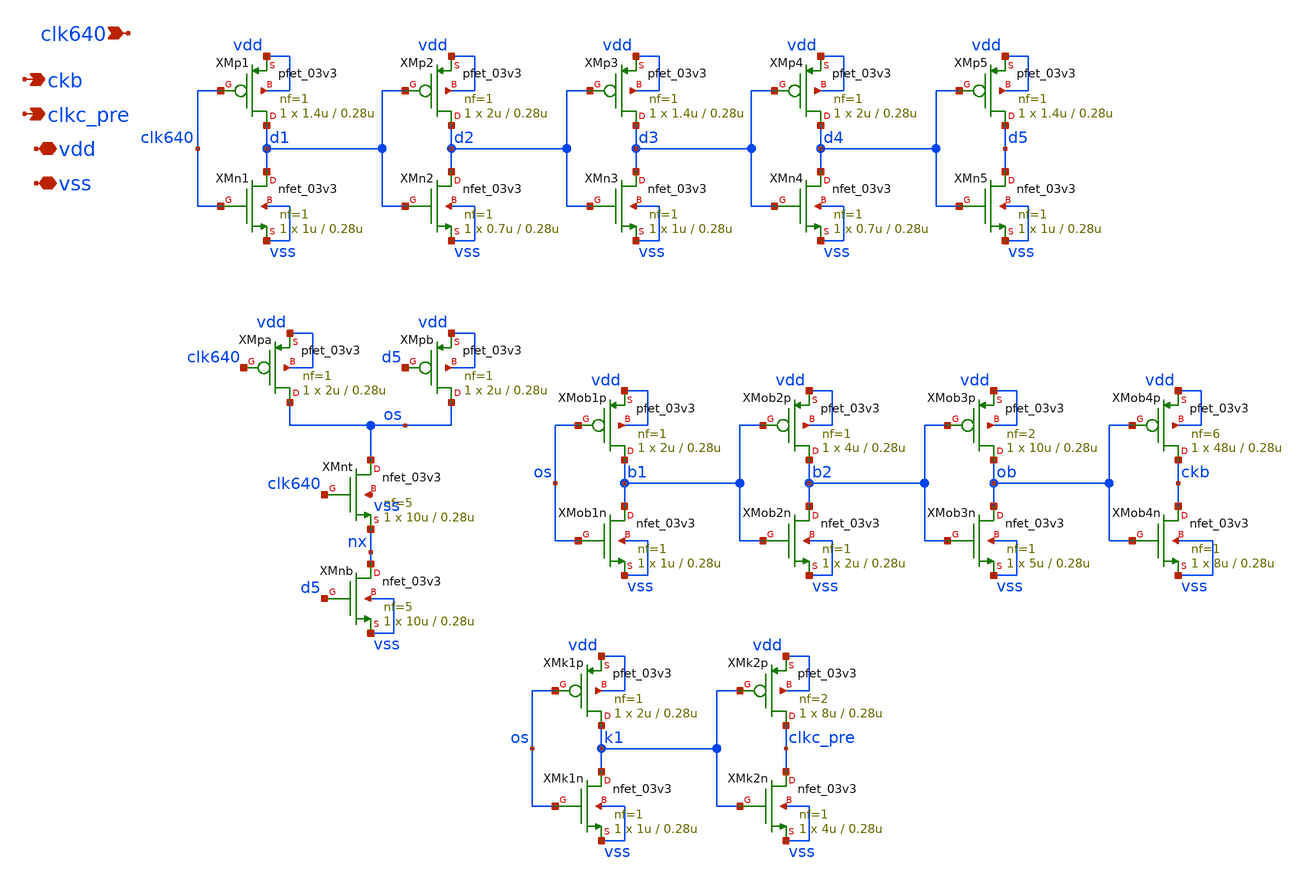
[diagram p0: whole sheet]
** sch_path: blocks/adc/comp-array/compact/clkshaper.sch
**.subckt clkshaper ckb vdd vss clkc_pre clk640
*.opin ckb
*.iopin vdd
*.iopin vss
*.opin clkc_pre
*.ipin clk640
XMn1 d1 clk640 vss vss nfet_03v3 L=0.28u W=1u nf=1 ad='int((nf+1)/2) * W/nf * 0.18u' as='int((nf+2)/2) * W/nf * 0.18u'
+ pd='2*int((nf+1)/2) * (W/nf + 0.18u)' ps='2*int((nf+2)/2) * (W/nf + 0.18u)' nrd='0.18u / W' nrs='0.18u / W'
+ sa=0 sb=0 sd=0 m=1
XMp1 d1 clk640 vdd vdd pfet_03v3 L=0.28u W=1.4u nf=1 ad='int((nf+1)/2) * W/nf * 0.18u' as='int((nf+2)/2) * W/nf * 0.18u'
+ pd='2*int((nf+1)/2) * (W/nf + 0.18u)' ps='2*int((nf+2)/2) * (W/nf + 0.18u)' nrd='0.18u / W' nrs='0.18u / W'
+ sa=0 sb=0 sd=0 m=1
XMn2 d2 d1 vss vss nfet_03v3 L=0.28u W=0.7u nf=1 ad='int((nf+1)/2) * W/nf * 0.18u' as='int((nf+2)/2) * W/nf * 0.18u'
+ pd='2*int((nf+1)/2) * (W/nf + 0.18u)' ps='2*int((nf+2)/2) * (W/nf + 0.18u)' nrd='0.18u / W' nrs='0.18u / W'
+ sa=0 sb=0 sd=0 m=1
XMp2 d2 d1 vdd vdd pfet_03v3 L=0.28u W=2u nf=1 ad='int((nf+1)/2) * W/nf * 0.18u' as='int((nf+2)/2) * W/nf * 0.18u'
+ pd='2*int((nf+1)/2) * (W/nf + 0.18u)' ps='2*int((nf+2)/2) * (W/nf + 0.18u)' nrd='0.18u / W' nrs='0.18u / W'
+ sa=0 sb=0 sd=0 m=1
XMn3 d3 d2 vss vss nfet_03v3 L=0.28u W=1u nf=1 ad='int((nf+1)/2) * W/nf * 0.18u' as='int((nf+2)/2) * W/nf * 0.18u'
+ pd='2*int((nf+1)/2) * (W/nf + 0.18u)' ps='2*int((nf+2)/2) * (W/nf + 0.18u)' nrd='0.18u / W' nrs='0.18u / W'
+ sa=0 sb=0 sd=0 m=1
XMp3 d3 d2 vdd vdd pfet_03v3 L=0.28u W=1.4u nf=1 ad='int((nf+1)/2) * W/nf * 0.18u' as='int((nf+2)/2) * W/nf * 0.18u'
+ pd='2*int((nf+1)/2) * (W/nf + 0.18u)' ps='2*int((nf+2)/2) * (W/nf + 0.18u)' nrd='0.18u / W' nrs='0.18u / W'
+ sa=0 sb=0 sd=0 m=1
XMn4 d4 d3 vss vss nfet_03v3 L=0.28u W=0.7u nf=1 ad='int((nf+1)/2) * W/nf * 0.18u' as='int((nf+2)/2) * W/nf * 0.18u'
+ pd='2*int((nf+1)/2) * (W/nf + 0.18u)' ps='2*int((nf+2)/2) * (W/nf + 0.18u)' nrd='0.18u / W' nrs='0.18u / W'
+ sa=0 sb=0 sd=0 m=1
XMp4 d4 d3 vdd vdd pfet_03v3 L=0.28u W=2u nf=1 ad='int((nf+1)/2) * W/nf * 0.18u' as='int((nf+2)/2) * W/nf * 0.18u'
+ pd='2*int((nf+1)/2) * (W/nf + 0.18u)' ps='2*int((nf+2)/2) * (W/nf + 0.18u)' nrd='0.18u / W' nrs='0.18u / W'
+ sa=0 sb=0 sd=0 m=1
XMn5 d5 d4 vss vss nfet_03v3 L=0.28u W=1u nf=1 ad='int((nf+1)/2) * W/nf * 0.18u' as='int((nf+2)/2) * W/nf * 0.18u'
+ pd='2*int((nf+1)/2) * (W/nf + 0.18u)' ps='2*int((nf+2)/2) * (W/nf + 0.18u)' nrd='0.18u / W' nrs='0.18u / W'
+ sa=0 sb=0 sd=0 m=1
XMp5 d5 d4 vdd vdd pfet_03v3 L=0.28u W=1.4u nf=1 ad='int((nf+1)/2) * W/nf * 0.18u' as='int((nf+2)/2) * W/nf * 0.18u'
+ pd='2*int((nf+1)/2) * (W/nf + 0.18u)' ps='2*int((nf+2)/2) * (W/nf + 0.18u)' nrd='0.18u / W' nrs='0.18u / W'
+ sa=0 sb=0 sd=0 m=1
XMpa os clk640 vdd vdd pfet_03v3 L=0.28u W=2u nf=1 ad='int((nf+1)/2) * W/nf * 0.18u' as='int((nf+2)/2) * W/nf * 0.18u'
+ pd='2*int((nf+1)/2) * (W/nf + 0.18u)' ps='2*int((nf+2)/2) * (W/nf + 0.18u)' nrd='0.18u / W' nrs='0.18u / W'
+ sa=0 sb=0 sd=0 m=1
XMpb os d5 vdd vdd pfet_03v3 L=0.28u W=2u nf=1 ad='int((nf+1)/2) * W/nf * 0.18u' as='int((nf+2)/2) * W/nf * 0.18u'
+ pd='2*int((nf+1)/2) * (W/nf + 0.18u)' ps='2*int((nf+2)/2) * (W/nf + 0.18u)' nrd='0.18u / W' nrs='0.18u / W'
+ sa=0 sb=0 sd=0 m=1
XMnt os clk640 nx vss nfet_03v3 L=0.28u W=10u nf=5 ad='int((nf+1)/2) * W/nf * 0.18u' as='int((nf+2)/2) * W/nf * 0.18u'
+ pd='2*int((nf+1)/2) * (W/nf + 0.18u)' ps='2*int((nf+2)/2) * (W/nf + 0.18u)' nrd='0.18u / W' nrs='0.18u / W'
+ sa=0 sb=0 sd=0 m=1
XMnb nx d5 vss vss nfet_03v3 L=0.28u W=10u nf=5 ad='int((nf+1)/2) * W/nf * 0.18u' as='int((nf+2)/2) * W/nf * 0.18u'
+ pd='2*int((nf+1)/2) * (W/nf + 0.18u)' ps='2*int((nf+2)/2) * (W/nf + 0.18u)' nrd='0.18u / W' nrs='0.18u / W'
+ sa=0 sb=0 sd=0 m=1
XMob1n b1 os vss vss nfet_03v3 L=0.28u W=1u nf=1 ad='int((nf+1)/2) * W/nf * 0.18u' as='int((nf+2)/2) * W/nf * 0.18u'
+ pd='2*int((nf+1)/2) * (W/nf + 0.18u)' ps='2*int((nf+2)/2) * (W/nf + 0.18u)' nrd='0.18u / W' nrs='0.18u / W'
+ sa=0 sb=0 sd=0 m=1
XMob1p b1 os vdd vdd pfet_03v3 L=0.28u W=2u nf=1 ad='int((nf+1)/2) * W/nf * 0.18u' as='int((nf+2)/2) * W/nf * 0.18u'
+ pd='2*int((nf+1)/2) * (W/nf + 0.18u)' ps='2*int((nf+2)/2) * (W/nf + 0.18u)' nrd='0.18u / W' nrs='0.18u / W'
+ sa=0 sb=0 sd=0 m=1
XMob2n b2 b1 vss vss nfet_03v3 L=0.28u W=2u nf=1 ad='int((nf+1)/2) * W/nf * 0.18u' as='int((nf+2)/2) * W/nf * 0.18u'
+ pd='2*int((nf+1)/2) * (W/nf + 0.18u)' ps='2*int((nf+2)/2) * (W/nf + 0.18u)' nrd='0.18u / W' nrs='0.18u / W'
+ sa=0 sb=0 sd=0 m=1
XMob2p b2 b1 vdd vdd pfet_03v3 L=0.28u W=4u nf=1 ad='int((nf+1)/2) * W/nf * 0.18u' as='int((nf+2)/2) * W/nf * 0.18u'
+ pd='2*int((nf+1)/2) * (W/nf + 0.18u)' ps='2*int((nf+2)/2) * (W/nf + 0.18u)' nrd='0.18u / W' nrs='0.18u / W'
+ sa=0 sb=0 sd=0 m=1
XMob3n ob b2 vss vss nfet_03v3 L=0.28u W=5u nf=1 ad='int((nf+1)/2) * W/nf * 0.18u' as='int((nf+2)/2) * W/nf * 0.18u'
+ pd='2*int((nf+1)/2) * (W/nf + 0.18u)' ps='2*int((nf+2)/2) * (W/nf + 0.18u)' nrd='0.18u / W' nrs='0.18u / W'
+ sa=0 sb=0 sd=0 m=1
XMob3p ob b2 vdd vdd pfet_03v3 L=0.28u W=10u nf=2 ad='int((nf+1)/2) * W/nf * 0.18u' as='int((nf+2)/2) * W/nf * 0.18u'
+ pd='2*int((nf+1)/2) * (W/nf + 0.18u)' ps='2*int((nf+2)/2) * (W/nf + 0.18u)' nrd='0.18u / W' nrs='0.18u / W'
+ sa=0 sb=0 sd=0 m=1
XMob4n ckb ob vss vss nfet_03v3 L=0.28u W=8u nf=1 ad='int((nf+1)/2) * W/nf * 0.18u' as='int((nf+2)/2) * W/nf * 0.18u'
+ pd='2*int((nf+1)/2) * (W/nf + 0.18u)' ps='2*int((nf+2)/2) * (W/nf + 0.18u)' nrd='0.18u / W' nrs='0.18u / W'
+ sa=0 sb=0 sd=0 m=1
XMob4p ckb ob vdd vdd pfet_03v3 L=0.28u W=48u nf=6 ad='int((nf+1)/2) * W/nf * 0.18u' as='int((nf+2)/2) * W/nf * 0.18u'
+ pd='2*int((nf+1)/2) * (W/nf + 0.18u)' ps='2*int((nf+2)/2) * (W/nf + 0.18u)' nrd='0.18u / W' nrs='0.18u / W'
+ sa=0 sb=0 sd=0 m=1
XMk1n k1 os vss vss nfet_03v3 L=0.28u W=1u nf=1 ad='int((nf+1)/2) * W/nf * 0.18u' as='int((nf+2)/2) * W/nf * 0.18u'
+ pd='2*int((nf+1)/2) * (W/nf + 0.18u)' ps='2*int((nf+2)/2) * (W/nf + 0.18u)' nrd='0.18u / W' nrs='0.18u / W'
+ sa=0 sb=0 sd=0 m=1
XMk1p k1 os vdd vdd pfet_03v3 L=0.28u W=2u nf=1 ad='int((nf+1)/2) * W/nf * 0.18u' as='int((nf+2)/2) * W/nf * 0.18u'
+ pd='2*int((nf+1)/2) * (W/nf + 0.18u)' ps='2*int((nf+2)/2) * (W/nf + 0.18u)' nrd='0.18u / W' nrs='0.18u / W'
+ sa=0 sb=0 sd=0 m=1
XMk2n clkc_pre k1 vss vss nfet_03v3 L=0.28u W=4u nf=1 ad='int((nf+1)/2) * W/nf * 0.18u' as='int((nf+2)/2) * W/nf * 0.18u'
+ pd='2*int((nf+1)/2) * (W/nf + 0.18u)' ps='2*int((nf+2)/2) * (W/nf + 0.18u)' nrd='0.18u / W' nrs='0.18u / W'
+ sa=0 sb=0 sd=0 m=1
XMk2p clkc_pre k1 vdd vdd pfet_03v3 L=0.28u W=8u nf=2 ad='int((nf+1)/2) * W/nf * 0.18u' as='int((nf+2)/2) * W/nf * 0.18u'
+ pd='2*int((nf+1)/2) * (W/nf + 0.18u)' ps='2*int((nf+2)/2) * (W/nf + 0.18u)' nrd='0.18u / W' nrs='0.18u / W'
+ sa=0 sb=0 sd=0 m=1
**.ends
.end
